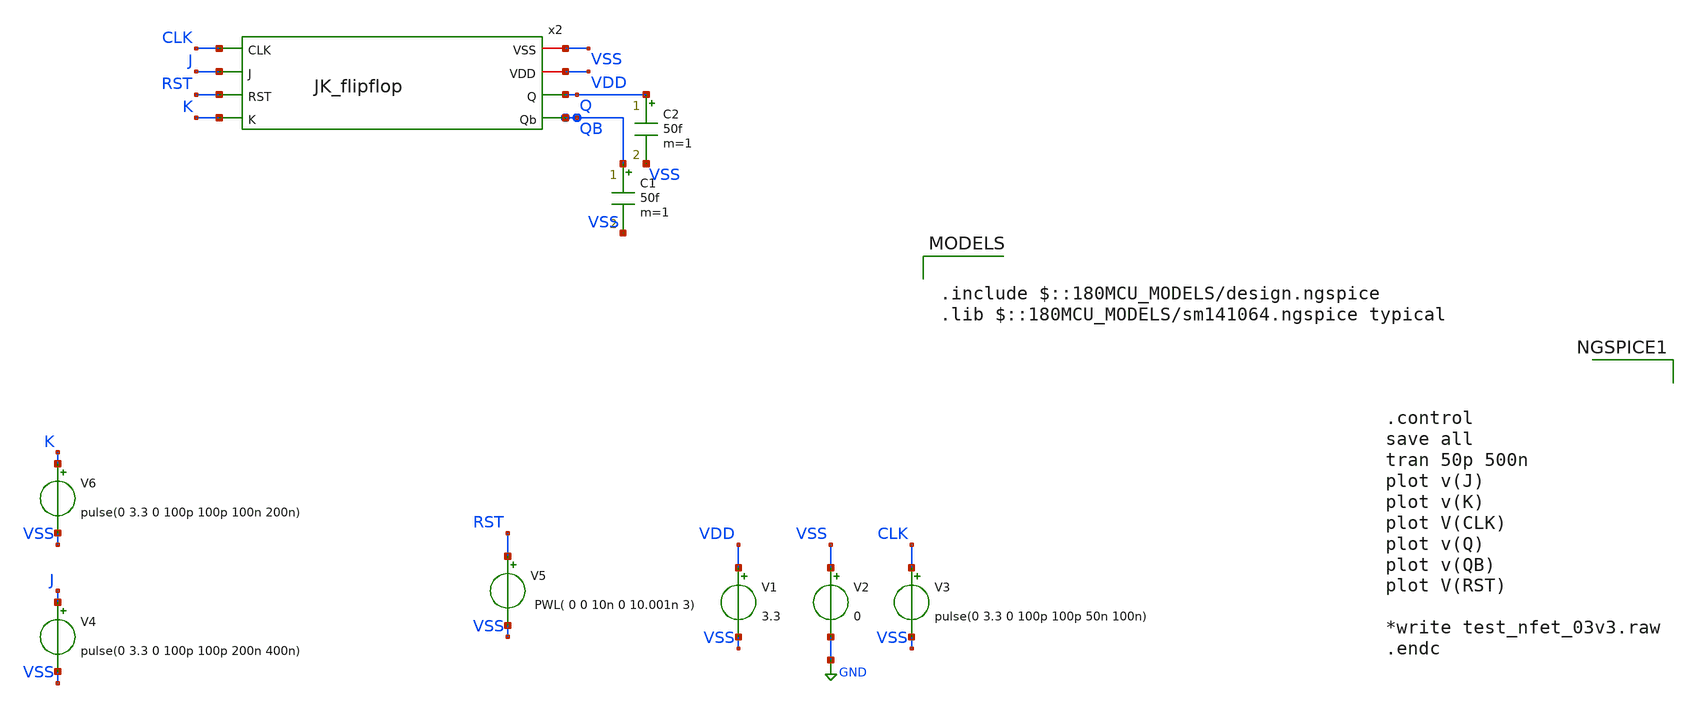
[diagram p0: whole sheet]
** sch_path: Clock_Generator_PAKISTAN_02/Schematics/JK_FF_TB.sch
**.subckt JK_FF_TB
V1 VDD VSS 3.3
V2 VSS GND 0
V3 CLK VSS pulse(0 3.3 0 100p 100p 50n 100n)
V4 J VSS pulse(0 3.3 0 100p 100p 200n 400n)
C1 QB VSS 50f m=1
C2 Q VSS 50f m=1
x2 CLK VSS VDD Q J QB RST K JK_flipflop
V6 K VSS pulse(0 3.3 0 100p 100p 100n 200n)
V5 RST VSS PWL( 0 0 10n 0 10.001n 3)
**** begin user architecture code

.include $::180MCU_MODELS/design.ngspice
.lib $::180MCU_MODELS/sm141064.ngspice typical




.control
save all
tran 50p 500n
plot v(J)
plot v(K)
plot V(CLK)
plot v(Q)
plot v(QB)
plot V(RST)

*write test_nfet_03v3.raw
.endc


**** end user architecture code
**.ends
.GLOBAL GND
.end
